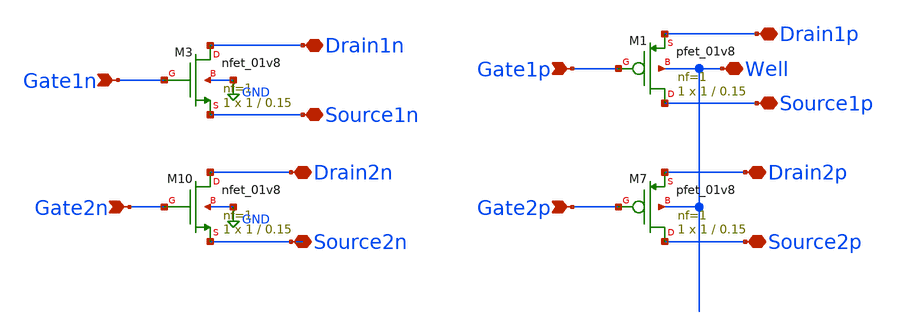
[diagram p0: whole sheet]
** sch_path: libs.ref/sky130_hilas_sc/xschem/sky130_hilas_Trans2med.sch
**.subckt sky130_hilas_Trans2med Gate2n Well Source2p Gate1n Drain1n Drain2n Gate2p Source1p Gate1p
*+ Drain1p Drain2p Source2n Source1n
*.ipin Gate2n
*.iopin Well
*.iopin Source2p
*.ipin Gate1n
*.iopin Drain1n
*.iopin Drain2n
*.ipin Gate2p
*.iopin Source1p
*.ipin Gate1p
*.iopin Drain1p
*.iopin Drain2p
*.iopin Source2n
*.iopin Source1n
XM1 Source1p Gate1p Drain1p Well sky130_fd_pr__pfet_01v8 L=0.15 W=1 nf=1 ad='int((nf+1)/2) * W/nf * 0.29'
+ as='int((nf+2)/2) * W/nf * 0.29' pd='2*int((nf+1)/2) * (W/nf + 0.29)' ps='2*int((nf+2)/2) * (W/nf + 0.29)'
+ nrd='0.29 / W' nrs='0.29 / W' sa=0 sb=0 sd=0 mult=1 m=1
XM3 Drain1n Gate1n Source1n GND sky130_fd_pr__nfet_01v8 L=0.15 W=1 nf=1 ad='int((nf+1)/2) * W/nf * 0.29'
+ as='int((nf+2)/2) * W/nf * 0.29' pd='2*int((nf+1)/2) * (W/nf + 0.29)' ps='2*int((nf+2)/2) * (W/nf + 0.29)'
+ nrd='0.29 / W' nrs='0.29 / W' sa=0 sb=0 sd=0 mult=1 m=1
XM7 Source2p Gate2p Drain2p Well sky130_fd_pr__pfet_01v8 L=0.15 W=1 nf=1 ad='int((nf+1)/2) * W/nf * 0.29'
+ as='int((nf+2)/2) * W/nf * 0.29' pd='2*int((nf+1)/2) * (W/nf + 0.29)' ps='2*int((nf+2)/2) * (W/nf + 0.29)'
+ nrd='0.29 / W' nrs='0.29 / W' sa=0 sb=0 sd=0 mult=1 m=1
XM10 Drain2n Gate2n Source2n GND sky130_fd_pr__nfet_01v8 L=0.15 W=1 nf=1 ad='int((nf+1)/2) * W/nf * 0.29'
+ as='int((nf+2)/2) * W/nf * 0.29' pd='2*int((nf+1)/2) * (W/nf + 0.29)' ps='2*int((nf+2)/2) * (W/nf + 0.29)'
+ nrd='0.29 / W' nrs='0.29 / W' sa=0 sb=0 sd=0 mult=1 m=1
**.ends
.GLOBAL GND
.end
